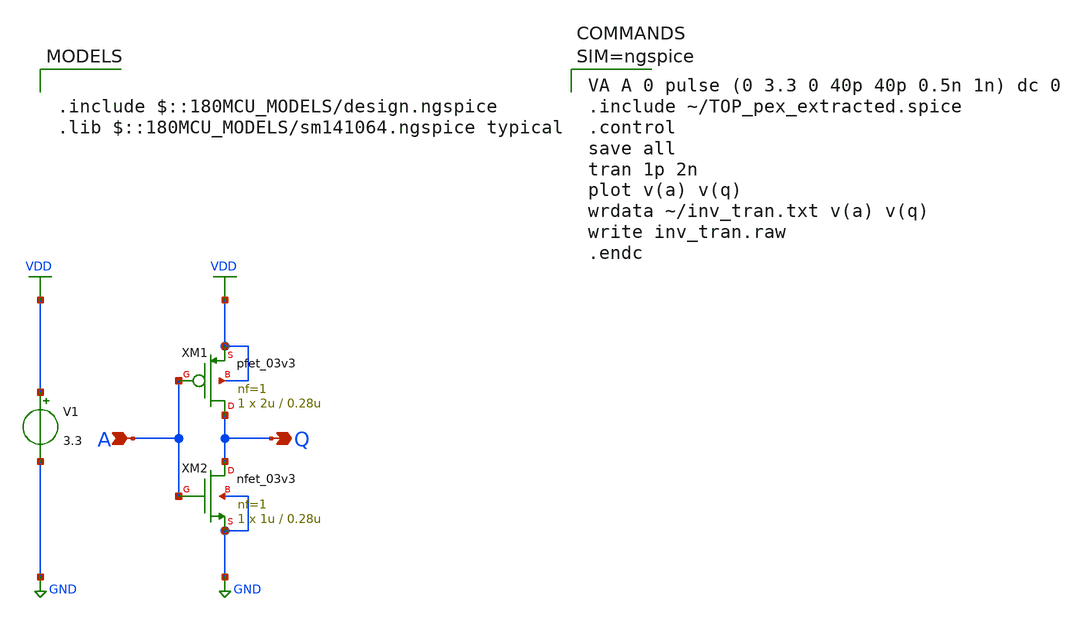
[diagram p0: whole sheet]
** sch_path: inv_tran.sch
**.subckt inv_tran Q A
*.opin Q
*.ipin A
XM1 Q A VDD VDD pfet_03v3 L=0.28u W=2u nf=1 ad='int((nf+1)/2) * W/nf * 0.18u' as='int((nf+2)/2) * W/nf * 0.18u'
+ pd='2*int((nf+1)/2) * (W/nf + 0.18u)' ps='2*int((nf+2)/2) * (W/nf + 0.18u)' nrd='0.18u / W' nrs='0.18u / W'
+ sa=0 sb=0 sd=0 m=1
XM2 Q A GND GND nfet_03v3 L=0.28u W=1u nf=1 ad='int((nf+1)/2) * W/nf * 0.18u' as='int((nf+2)/2) * W/nf * 0.18u'
+ pd='2*int((nf+1)/2) * (W/nf + 0.18u)' ps='2*int((nf+2)/2) * (W/nf + 0.18u)' nrd='0.18u / W' nrs='0.18u / W'
+ sa=0 sb=0 sd=0 m=1
V1 VDD GND 3.3
**** begin user architecture code

.include $::180MCU_MODELS/design.ngspice
.lib $::180MCU_MODELS/sm141064.ngspice typical



VA A 0 pulse (0 3.3 0 40p 40p 0.5n 1n) dc 0
.include ~/TOP_pex_extracted.spice
.control
save all
tran 1p 2n
plot v(a) v(q)
wrdata ~/inv_tran.txt v(a) v(q)
write inv_tran.raw
.endc



**** end user architecture code
**.ends
.GLOBAL VDD
.GLOBAL GND
.end
